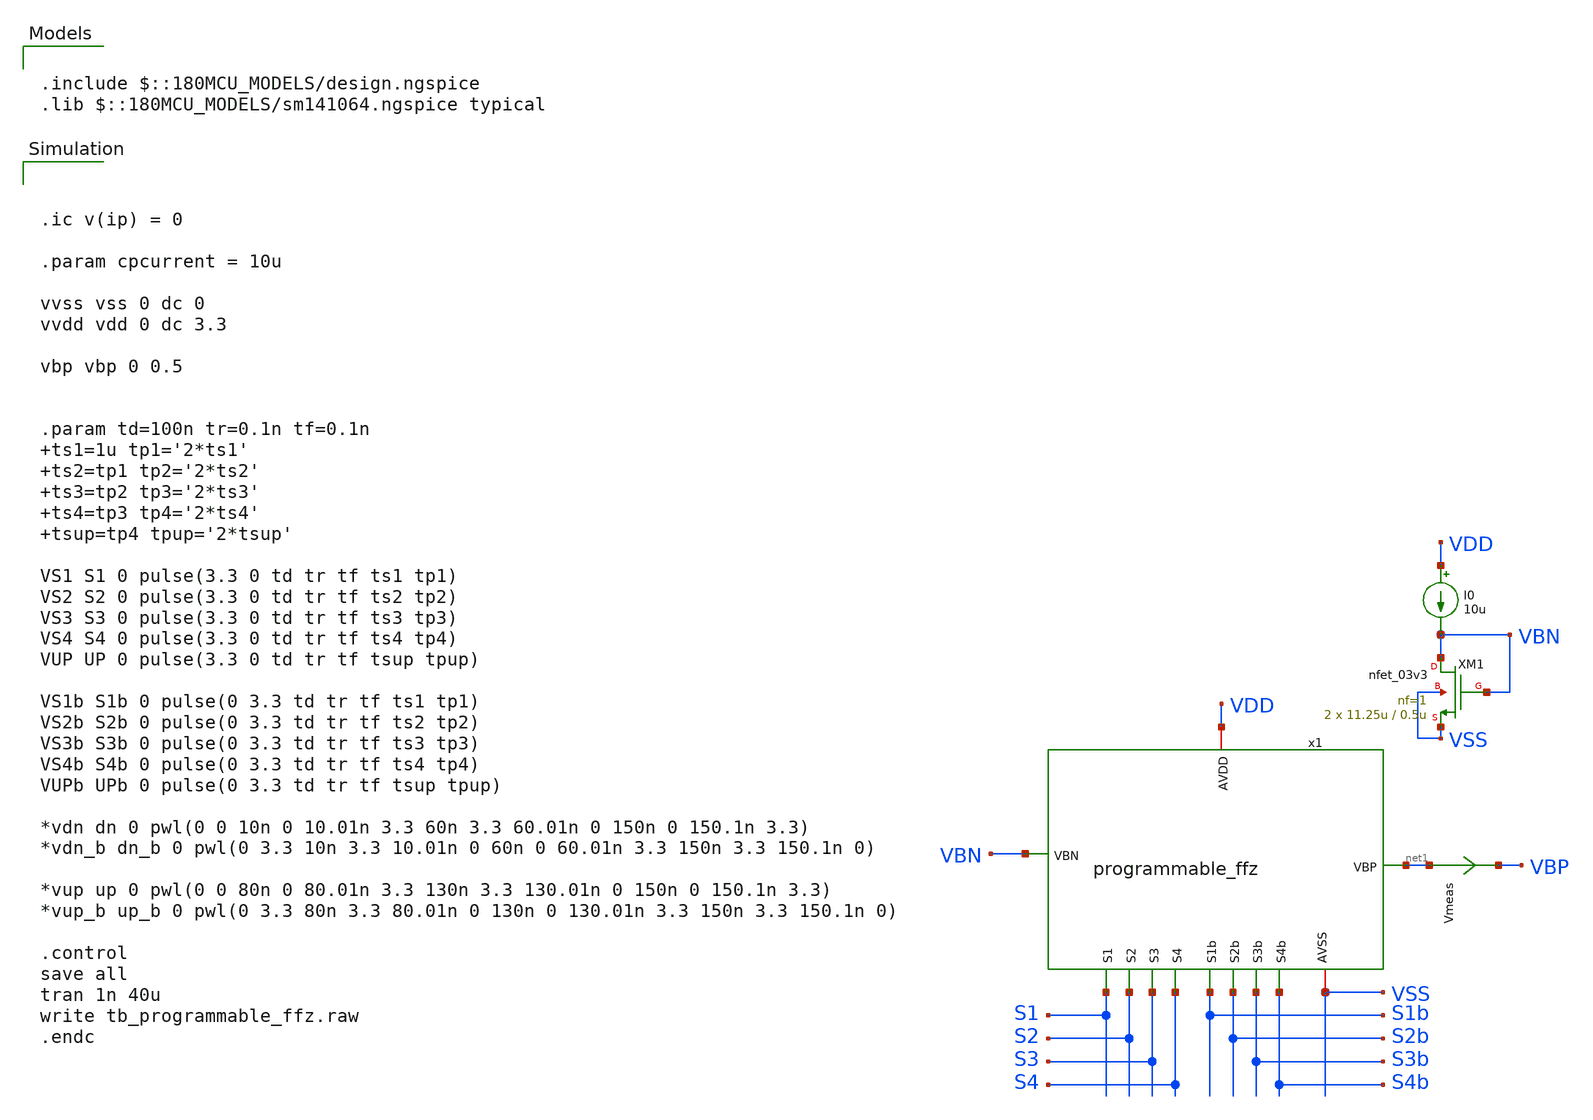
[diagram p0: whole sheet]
** sch_path: designs/libs/tb_analog/tb_programmable_ffz/tb_programmable_ffz.sch
**.subckt tb_programmable_ffz
Vmeas net1 VBP 0
.save i(vmeas)
XM1 VBN VBN VSS VSS nfet_03v3 L=0.5u W=11.25u nf=1 ad='int((nf+1)/2) * W/nf * 0.18u' as='int((nf+2)/2) * W/nf * 0.18u'
+ pd='2*int((nf+1)/2) * (W/nf + 0.18u)' ps='2*int((nf+2)/2) * (W/nf + 0.18u)' nrd='0.18u / W' nrs='0.18u / W'
+ sa=0 sb=0 sd=0 m=2
I0 VDD VBN 10u
x1 net1 VSS VDD VBN S1b S1 S2b S2 S3b S3 S4b S4 programmable_ffz
**** begin user architecture code



.ic v(ip) = 0

.param cpcurrent = 10u

vvss vss 0 dc 0
vvdd vdd 0 dc 3.3

vbp vbp 0 0.5


.param td=100n tr=0.1n tf=0.1n ts1=1u tp1='2*ts1' ts2=tp1 tp2='2*ts2' ts3=tp2 tp3='2*ts3' ts4=tp3 tp4='2*ts4'
+ tsup=tp4 tpup='2*tsup'

VS1 S1 0 pulse(3.3 0 td tr tf ts1 tp1)
VS2 S2 0 pulse(3.3 0 td tr tf ts2 tp2)
VS3 S3 0 pulse(3.3 0 td tr tf ts3 tp3)
VS4 S4 0 pulse(3.3 0 td tr tf ts4 tp4)
VUP UP 0 pulse(3.3 0 td tr tf tsup tpup)

VS1b S1b 0 pulse(0 3.3 td tr tf ts1 tp1)
VS2b S2b 0 pulse(0 3.3 td tr tf ts2 tp2)
VS3b S3b 0 pulse(0 3.3 td tr tf ts3 tp3)
VS4b S4b 0 pulse(0 3.3 td tr tf ts4 tp4)
VUPb UPb 0 pulse(0 3.3 td tr tf tsup tpup)

*vdn dn 0 pwl(0 0 10n 0 10.01n 3.3 60n 3.3 60.01n 0 150n 0 150.1n 3.3)
*vdn_b dn_b 0 pwl(0 3.3 10n 3.3 10.01n 0 60n 0 60.01n 3.3 150n 3.3 150.1n 0)

*vup up 0 pwl(0 0 80n 0 80.01n 3.3 130n 3.3 130.01n 0 150n 0 150.1n 3.3)
*vup_b up_b 0 pwl(0 3.3 80n 3.3 80.01n 0 130n 0 130.01n 3.3 150n 3.3 150.1n 0)

.control
save all
tran 1n 40u
write tb_programmable_ffz.raw
.endc



.include $::180MCU_MODELS/design.ngspice
.lib $::180MCU_MODELS/sm141064.ngspice typical

**** end user architecture code
**.ends

* expanding   symbol:  libs/core_analog/programmable_ffz/programmable_ffz.sym # of pins=12
** sym_path: designs/libs/core_analog/programmable_ffz/programmable_ffz.sym
** sch_path: designs/libs/core_analog/programmable_ffz/programmable_ffz.sch
.subckt programmable_ffz VBP AVSS AVDD VBN S1b S1 S2b S2 S3b S3 S4b S4
*.ipin VBN
*.ipin S1b
*.ipin S1
*.ipin S2b
*.ipin S2
*.ipin S3b
*.ipin S3
*.ipin S4b
*.ipin S4
*.iopin AVSS
*.iopin AVDD
*.opin VBP
x2 VBN AVSS S1 VBN1 S1b AVDD transmission_gate
x3 VBN AVSS S2 VBN2 S2b AVDD transmission_gate
x4 VBN AVSS S3 VBN3 S3b AVDD transmission_gate
x5 VBN AVSS S4 VBN4 S4b AVDD transmission_gate
x1 AVDD VBP VBN AVSS AVSS feed_forward_zero
x6 AVDD net1 VBN1 S1b AVSS feed_forward_zero
x71 AVDD net2[1] VBN2 S2b AVSS feed_forward_zero
x72 AVDD net2[0] VBN2 S2b AVSS feed_forward_zero
x11 AVDD net3[3] VBN3 S3b AVSS feed_forward_zero
x12 AVDD net3[2] VBN3 S3b AVSS feed_forward_zero
x13 AVDD net3[1] VBN3 S3b AVSS feed_forward_zero
x14 AVDD net3[0] VBN3 S3b AVSS feed_forward_zero
x21 AVDD net4[7] VBN4 S4b AVSS feed_forward_zero
x22 AVDD net4[6] VBN4 S4b AVSS feed_forward_zero
x23 AVDD net4[5] VBN4 S4b AVSS feed_forward_zero
x24 AVDD net4[4] VBN4 S4b AVSS feed_forward_zero
x25 AVDD net4[3] VBN4 S4b AVSS feed_forward_zero
x26 AVDD net4[2] VBN4 S4b AVSS feed_forward_zero
x27 AVDD net4[1] VBN4 S4b AVSS feed_forward_zero
x28 AVDD net4[0] VBN4 S4b AVSS feed_forward_zero
x7 net1 AVSS S1 VBP S1b AVDD transmission_gate
x81 net2[1] AVSS S2 VBP S2b AVDD transmission_gate
x82 net2[0] AVSS S2 VBP S2b AVDD transmission_gate
x91 net3[3] AVSS S3 VBP S3b AVDD transmission_gate
x92 net3[2] AVSS S3 VBP S3b AVDD transmission_gate
x93 net3[1] AVSS S3 VBP S3b AVDD transmission_gate
x94 net3[0] AVSS S3 VBP S3b AVDD transmission_gate
x101 net4[7] AVSS S4 VBP S4b AVDD transmission_gate
x102 net4[6] AVSS S4 VBP S4b AVDD transmission_gate
x103 net4[5] AVSS S4 VBP S4b AVDD transmission_gate
x104 net4[4] AVSS S4 VBP S4b AVDD transmission_gate
x105 net4[3] AVSS S4 VBP S4b AVDD transmission_gate
x106 net4[2] AVSS S4 VBP S4b AVDD transmission_gate
x107 net4[1] AVSS S4 VBP S4b AVDD transmission_gate
x108 net4[0] AVSS S4 VBP S4b AVDD transmission_gate
.ends


* expanding   symbol:  libs/core_analog/transmission_gate/transmission_gate.sym # of pins=6
** sym_path: designs/libs/core_analog/transmission_gate/transmission_gate.sym
** sch_path: designs/libs/core_analog/transmission_gate/transmission_gate.sch
.subckt transmission_gate ind vss clkn ins clkp vdd
*.iopin ind
*.iopin ins
*.iopin clkn
*.iopin clkp
*.iopin vdd
*.iopin vss
XM1 ind clkp ins vdd pfet_03v3 L=0.5u W=3.0u nf=1 ad='int((nf+1)/2) * W/nf * 0.18u' as='int((nf+2)/2) * W/nf * 0.18u'
+ pd='2*int((nf+1)/2) * (W/nf + 0.18u)' ps='2*int((nf+2)/2) * (W/nf + 0.18u)' nrd='0.18u / W' nrs='0.18u / W'
+ sa=0 sb=0 sd=0 m=1
XM2 ind clkn ins vss nfet_03v3 L=0.5u W=1.0u nf=1 ad='int((nf+1)/2) * W/nf * 0.18u' as='int((nf+2)/2) * W/nf * 0.18u'
+ pd='2*int((nf+1)/2) * (W/nf + 0.18u)' ps='2*int((nf+2)/2) * (W/nf + 0.18u)' nrd='0.18u / W' nrs='0.18u / W'
+ sa=0 sb=0 sd=0 m=1
.ends


* expanding   symbol:  libs/core_analog/feed_forward_zero/feed_forward_zero.sym # of pins=5
** sym_path: designs/libs/core_analog/feed_forward_zero/feed_forward_zero.sym
** sch_path: designs/libs/core_analog/feed_forward_zero/feed_forward_zero.sch
.subckt feed_forward_zero AVDD VBP VBN S AVSS
*.opin VBP
*.iopin AVDD
*.iopin AVSS
*.ipin VBN
*.ipin S
XM1 VBP VBP AVDD AVDD pfet_03v3 L=1.5u W=1.1u nf=1 ad='int((nf+1)/2) * W/nf * 0.18u' as='int((nf+2)/2) * W/nf * 0.18u'
+ pd='2*int((nf+1)/2) * (W/nf + 0.18u)' ps='2*int((nf+2)/2) * (W/nf + 0.18u)' nrd='0.18u / W' nrs='0.18u / W'
+ sa=0 sb=0 sd=0 m=2
XM2 VBP VBP AVDD AVDD pfet_03v3 L=1.5u W=1.1u nf=1 ad='int((nf+1)/2) * W/nf * 0.18u' as='int((nf+2)/2) * W/nf * 0.18u'
+ pd='2*int((nf+1)/2) * (W/nf + 0.18u)' ps='2*int((nf+2)/2) * (W/nf + 0.18u)' nrd='0.18u / W' nrs='0.18u / W'
+ sa=0 sb=0 sd=0 m=2
XM3 VBP AVDD net1 AVSS nfet_03v3 L=0.5u W=2.08u nf=1 ad='int((nf+1)/2) * W/nf * 0.18u' as='int((nf+2)/2) * W/nf * 0.18u'
+ pd='2*int((nf+1)/2) * (W/nf + 0.18u)' ps='2*int((nf+2)/2) * (W/nf + 0.18u)' nrd='0.18u / W' nrs='0.18u / W'
+ sa=0 sb=0 sd=0 m=2
XM4 net1 VBN AVSS AVSS nfet_03v3 L=0.5u W=11.25u nf=1 ad='int((nf+1)/2) * W/nf * 0.18u' as='int((nf+2)/2) * W/nf * 0.18u'
+ pd='2*int((nf+1)/2) * (W/nf + 0.18u)' ps='2*int((nf+2)/2) * (W/nf + 0.18u)' nrd='0.18u / W' nrs='0.18u / W'
+ sa=0 sb=0 sd=0 m=2
XM7 VBN S AVSS AVSS nfet_03v3 L=0.5u W=1u nf=1 ad='int((nf+1)/2) * W/nf * 0.18u' as='int((nf+2)/2) * W/nf * 0.18u'
+ pd='2*int((nf+1)/2) * (W/nf + 0.18u)' ps='2*int((nf+2)/2) * (W/nf + 0.18u)' nrd='0.18u / W' nrs='0.18u / W'
+ sa=0 sb=0 sd=0 m=1
.ends

.end
